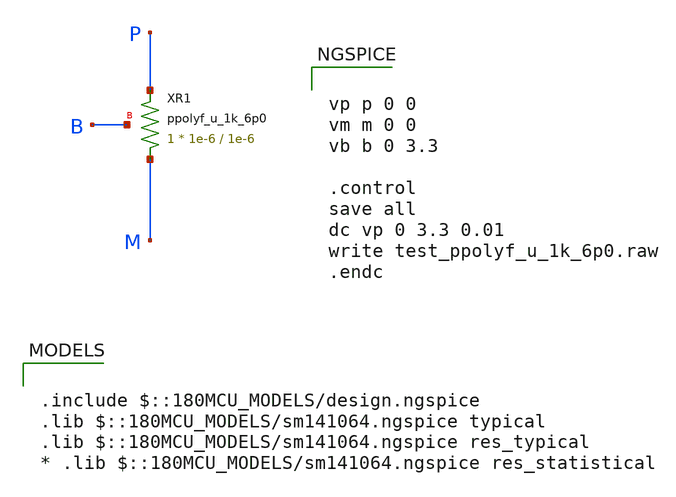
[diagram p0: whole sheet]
** sch_path: gf180mcuD/xschem_libs/gf180mcu_tests/test_ppolyf_u_1k_6p0/schematic/test_ppolyf_u_1k_6p0.sch
* Copyright 2022 GlobalFoundries PDK Authors
* Licensed under the Apache License, Version 2.0 (the "License");
* you may not use this file except in compliance with the License.
* You may obtain a copy of the License at
* https://www.apache.org/licenses/LICENSE-2.0
* Unless required by applicable law or agreed to in writing, software
* distributed under the License is distributed on an "AS IS" BASIS,
* WITHOUT WARRANTIES OR CONDITIONS OF ANY KIND, either express or implied.
* See the License for the specific language governing permissions and
* limitations under the License.
**.subckt test_ppolyf_u_1k_6p0
XR1 M P B ppolyf_u_1k_6p0 r_width=1e-6 r_length=1e-6 m=1
**** begin user architecture code

.include $::180MCU_MODELS/design.ngspice
.lib $::180MCU_MODELS/sm141064.ngspice typical
.lib $::180MCU_MODELS/sm141064.ngspice res_typical
* .lib $::180MCU_MODELS/sm141064.ngspice res_statistical



vp p 0 0
vm m 0 0
vb b 0 3.3

.control
save all
dc vp 0 3.3 0.01
write test_ppolyf_u_1k_6p0.raw
.endc


**** end user architecture code
**.ends
.end
